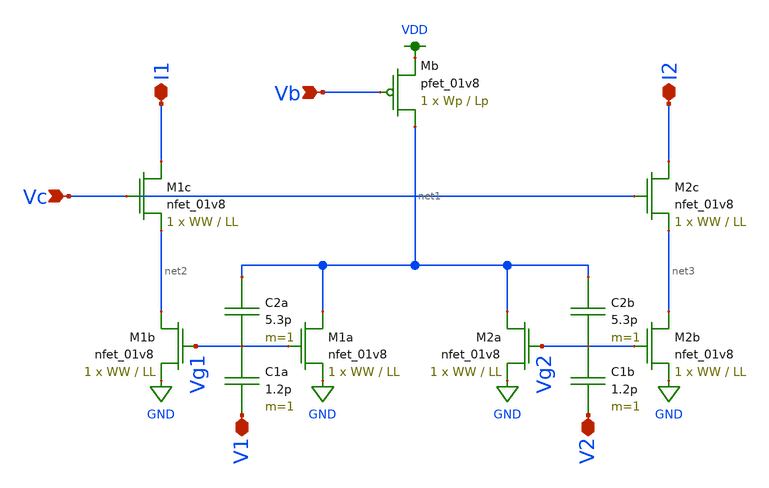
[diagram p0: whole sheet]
** sch_path: schematic/fgmos_diffpair.sch
**.subckt fgmos_diffpair Vb Vc V1 V2 I1 I2
*.ipin Vb
*.ipin Vc
*.iopin V1
*.iopin V2
*.iopin I1
*.iopin I2
XM1a net1 Vg1 GND GND sky130_fd_pr__nfet_01v8 L=LL W=WW nf=1 ad='int((nf+1)/2) * W/nf * 0.29' as='int((nf+2)/2) * W/nf * 0.29'
+ pd='2*int((nf+1)/2) * (W/nf + 0.29)' ps='2*int((nf+2)/2) * (W/nf + 0.29)' nrd='0.29 / W' nrs='0.29 / W'
+ sa=0 sb=0 sd=0 mult=1 m=1
XM1b net2 Vg1 GND GND sky130_fd_pr__nfet_01v8 L=LL W=WW nf=1 ad='int((nf+1)/2) * W/nf * 0.29' as='int((nf+2)/2) * W/nf * 0.29'
+ pd='2*int((nf+1)/2) * (W/nf + 0.29)' ps='2*int((nf+2)/2) * (W/nf + 0.29)' nrd='0.29 / W' nrs='0.29 / W'
+ sa=0 sb=0 sd=0 mult=1 m=1
XM1c I1 Vc net2 GND sky130_fd_pr__nfet_01v8 L=LL W=WW nf=1 ad='int((nf+1)/2) * W/nf * 0.29' as='int((nf+2)/2) * W/nf * 0.29'
+ pd='2*int((nf+1)/2) * (W/nf + 0.29)' ps='2*int((nf+2)/2) * (W/nf + 0.29)' nrd='0.29 / W' nrs='0.29 / W'
+ sa=0 sb=0 sd=0 mult=1 m=1
XM2b net3 Vg2 GND GND sky130_fd_pr__nfet_01v8 L=LL W=WW nf=1 ad='int((nf+1)/2) * W/nf * 0.29' as='int((nf+2)/2) * W/nf * 0.29'
+ pd='2*int((nf+1)/2) * (W/nf + 0.29)' ps='2*int((nf+2)/2) * (W/nf + 0.29)' nrd='0.29 / W' nrs='0.29 / W'
+ sa=0 sb=0 sd=0 mult=1 m=1
XM2a net1 Vg2 GND GND sky130_fd_pr__nfet_01v8 L=LL W=WW nf=1 ad='int((nf+1)/2) * W/nf * 0.29' as='int((nf+2)/2) * W/nf * 0.29'
+ pd='2*int((nf+1)/2) * (W/nf + 0.29)' ps='2*int((nf+2)/2) * (W/nf + 0.29)' nrd='0.29 / W' nrs='0.29 / W'
+ sa=0 sb=0 sd=0 mult=1 m=1
XM2c I2 Vc net3 GND sky130_fd_pr__nfet_01v8 L=LL W=WW nf=1 ad='int((nf+1)/2) * W/nf * 0.29' as='int((nf+2)/2) * W/nf * 0.29'
+ pd='2*int((nf+1)/2) * (W/nf + 0.29)' ps='2*int((nf+2)/2) * (W/nf + 0.29)' nrd='0.29 / W' nrs='0.29 / W'
+ sa=0 sb=0 sd=0 mult=1 m=1
XMb net1 Vb VDD VDD sky130_fd_pr__pfet_01v8 L=Lp W=Wp nf=1 ad='int((nf+1)/2) * W/nf * 0.29' as='int((nf+2)/2) * W/nf * 0.29'
+ pd='2*int((nf+1)/2) * (W/nf + 0.29)' ps='2*int((nf+2)/2) * (W/nf + 0.29)' nrd='0.29 / W' nrs='0.29 / W'
+ sa=0 sb=0 sd=0 mult=1 m=1
C2b net1 Vg2 5.3p m=1
C1a Vg1 V1 1.2p m=1
C1b Vg2 V2 1.2p m=1
C2a net1 Vg1 5.3p m=1
**.ends
.GLOBAL VDD
.GLOBAL GND
.end
